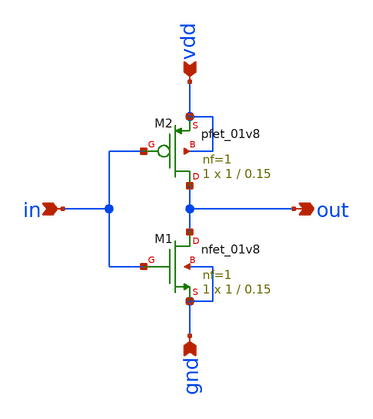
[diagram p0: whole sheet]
** sch_path: xschem/attenuator/basic-invert.sch
**.subckt basic-invert in gnd vdd out
*.ipin in
*.ipin gnd
*.ipin vdd
*.opin out
XM1 out in gnd gnd sky130_fd_pr__nfet_01v8 L=0.15 W=1 nf=1 ad='int((nf+1)/2) * W/nf * 0.29' as='int((nf+2)/2) * W/nf * 0.29'
+ pd='2*int((nf+1)/2) * (W/nf + 0.29)' ps='2*int((nf+2)/2) * (W/nf + 0.29)' nrd='0.29 / W' nrs='0.29 / W'
+ sa=0 sb=0 sd=0 mult=1 m=1
XM2 out in vdd vdd sky130_fd_pr__pfet_01v8 L=0.15 W=1 nf=1 ad='int((nf+1)/2) * W/nf * 0.29' as='int((nf+2)/2) * W/nf * 0.29'
+ pd='2*int((nf+1)/2) * (W/nf + 0.29)' ps='2*int((nf+2)/2) * (W/nf + 0.29)' nrd='0.29 / W' nrs='0.29 / W'
+ sa=0 sb=0 sd=0 mult=1 m=1
**.ends
.end
